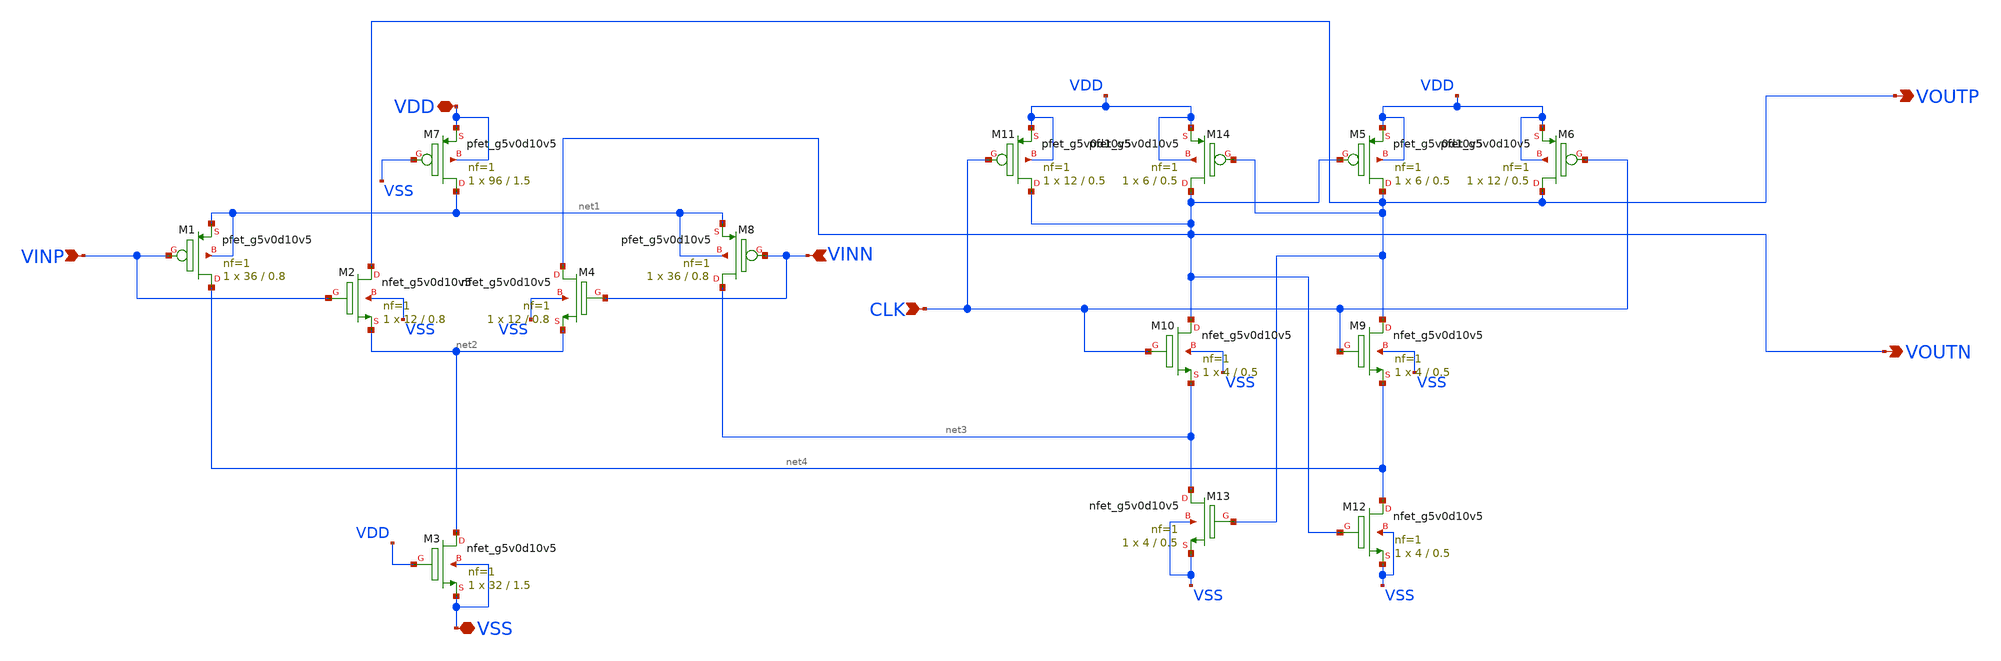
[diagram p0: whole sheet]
** sch_path: SKY130/SAR-ADC/SAR-ADC_5.0V/comp.sch
**.subckt comp VOUTP VOUTN VINP VINN CLK VDD VSS
*.opin VOUTP
*.opin VOUTN
*.ipin VINP
*.ipin VINN
*.ipin CLK
*.iopin VDD
*.iopin VSS
XM8 net3 VINN net1 net1 sky130_fd_pr__pfet_g5v0d10v5 L=0.8 W=36 nf=1 ad='int((1 + 1)/2) * 36 / 1 * 0.29'
+ as='int((1 + 2)/2) * 36 / 1 * 0.29' pd='2*int((1 + 1)/2) * (36 / 1 + 0.29)' ps='2*int((1 + 2)/2) * (36 / 1 + 0.29)'
+ nrd='0.29 / 36 ' nrs='0.29 / 36 ' sa=0 sb=0 sd=0 mult=1 m=1
XM7 net1 VSS VDD VDD sky130_fd_pr__pfet_g5v0d10v5 L=1.5 W=96 nf=1 ad='int((1 + 1)/2) * 96 / 1 * 0.29'
+ as='int((1 + 2)/2) * 96 / 1 * 0.29' pd='2*int((1 + 1)/2) * (96 / 1 + 0.29)' ps='2*int((1 + 2)/2) * (96 / 1 + 0.29)'
+ nrd='0.29 / 96 ' nrs='0.29 / 96 ' sa=0 sb=0 sd=0 mult=1 m=1
XM1 net4 VINP net1 net1 sky130_fd_pr__pfet_g5v0d10v5 L=0.8 W=36 nf=1 ad='int((1 + 1)/2) * 36 / 1 * 0.29'
+ as='int((1 + 2)/2) * 36 / 1 * 0.29' pd='2*int((1 + 1)/2) * (36 / 1 + 0.29)' ps='2*int((1 + 2)/2) * (36 / 1 + 0.29)'
+ nrd='0.29 / 36 ' nrs='0.29 / 36 ' sa=0 sb=0 sd=0 mult=1 m=1
XM2 VOUTP VINP net2 VSS sky130_fd_pr__nfet_g5v0d10v5 L=0.8 W=12 nf=1 ad='int((1 + 1)/2) * 12 / 1 * 0.29'
+ as='int((1 + 2)/2) * 12 / 1 * 0.29' pd='2*int((1 + 1)/2) * (12 / 1 + 0.29)' ps='2*int((1 + 2)/2) * (12 / 1 + 0.29)'
+ nrd='0.29 / 12 ' nrs='0.29 / 12 ' sa=0 sb=0 sd=0 mult=1 m=1
XM3 net2 VDD VSS VSS sky130_fd_pr__nfet_g5v0d10v5 L=1.5 W=32 nf=1 ad='int((1 + 1)/2) * 32 / 1 * 0.29'
+ as='int((1 + 2)/2) * 32 / 1 * 0.29' pd='2*int((1 + 1)/2) * (32 / 1 + 0.29)' ps='2*int((1 + 2)/2) * (32 / 1 + 0.29)'
+ nrd='0.29 / 32 ' nrs='0.29 / 32 ' sa=0 sb=0 sd=0 mult=1 m=1
XM4 VOUTN VINN net2 VSS sky130_fd_pr__nfet_g5v0d10v5 L=0.8 W=12 nf=1 ad='int((1 + 1)/2) * 12 / 1 * 0.29'
+ as='int((1 + 2)/2) * 12 / 1 * 0.29' pd='2*int((1 + 1)/2) * (12 / 1 + 0.29)' ps='2*int((1 + 2)/2) * (12 / 1 + 0.29)'
+ nrd='0.29 / 12 ' nrs='0.29 / 12 ' sa=0 sb=0 sd=0 mult=1 m=1
XM9 VOUTP CLK net4 VSS sky130_fd_pr__nfet_g5v0d10v5 L=0.5 W=4 nf=1 ad='int((1 + 1)/2) * 4 / 1 * 0.29'
+ as='int((1 + 2)/2) * 4 / 1 * 0.29' pd='2*int((1 + 1)/2) * (4 / 1 + 0.29)' ps='2*int((1 + 2)/2) * (4 / 1 + 0.29)'
+ nrd='0.29 / 4 ' nrs='0.29 / 4 ' sa=0 sb=0 sd=0 mult=1 m=1
XM10 VOUTN CLK net3 VSS sky130_fd_pr__nfet_g5v0d10v5 L=0.5 W=4 nf=1 ad='int((1 + 1)/2) * 4 / 1 * 0.29'
+ as='int((1 + 2)/2) * 4 / 1 * 0.29' pd='2*int((1 + 1)/2) * (4 / 1 + 0.29)' ps='2*int((1 + 2)/2) * (4 / 1 + 0.29)'
+ nrd='0.29 / 4 ' nrs='0.29 / 4 ' sa=0 sb=0 sd=0 mult=1 m=1
XM12 net4 VOUTN VSS VSS sky130_fd_pr__nfet_g5v0d10v5 L=0.5 W=4 nf=1 ad='int((1 + 1)/2) * 4 / 1 * 0.29'
+ as='int((1 + 2)/2) * 4 / 1 * 0.29' pd='2*int((1 + 1)/2) * (4 / 1 + 0.29)' ps='2*int((1 + 2)/2) * (4 / 1 + 0.29)'
+ nrd='0.29 / 4 ' nrs='0.29 / 4 ' sa=0 sb=0 sd=0 mult=1 m=1
XM13 net3 VOUTP VSS VSS sky130_fd_pr__nfet_g5v0d10v5 L=0.5 W=4 nf=1 ad='int((1 + 1)/2) * 4 / 1 * 0.29'
+ as='int((1 + 2)/2) * 4 / 1 * 0.29' pd='2*int((1 + 1)/2) * (4 / 1 + 0.29)' ps='2*int((1 + 2)/2) * (4 / 1 + 0.29)'
+ nrd='0.29 / 4 ' nrs='0.29 / 4 ' sa=0 sb=0 sd=0 mult=1 m=1
XM14 VOUTN VOUTP VDD VDD sky130_fd_pr__pfet_g5v0d10v5 L=0.5 W=6 nf=1 ad='int((1 + 1)/2) * 6 / 1 * 0.29'
+ as='int((1 + 2)/2) * 6 / 1 * 0.29' pd='2*int((1 + 1)/2) * (6 / 1 + 0.29)' ps='2*int((1 + 2)/2) * (6 / 1 + 0.29)'
+ nrd='0.29 / 6 ' nrs='0.29 / 6 ' sa=0 sb=0 sd=0 mult=1 m=1
XM11 VOUTN CLK VDD VDD sky130_fd_pr__pfet_g5v0d10v5 L=0.5 W=12 nf=1 ad='int((1 + 1)/2) * 12 / 1 * 0.29'
+ as='int((1 + 2)/2) * 12 / 1 * 0.29' pd='2*int((1 + 1)/2) * (12 / 1 + 0.29)' ps='2*int((1 + 2)/2) * (12 / 1 + 0.29)'
+ nrd='0.29 / 12 ' nrs='0.29 / 12 ' sa=0 sb=0 sd=0 mult=1 m=1
XM5 VOUTP VOUTN VDD VDD sky130_fd_pr__pfet_g5v0d10v5 L=0.5 W=6 nf=1 ad='int((1 + 1)/2) * 6 / 1 * 0.29'
+ as='int((1 + 2)/2) * 6 / 1 * 0.29' pd='2*int((1 + 1)/2) * (6 / 1 + 0.29)' ps='2*int((1 + 2)/2) * (6 / 1 + 0.29)'
+ nrd='0.29 / 6 ' nrs='0.29 / 6 ' sa=0 sb=0 sd=0 mult=1 m=1
XM6 VOUTP CLK VDD VDD sky130_fd_pr__pfet_g5v0d10v5 L=0.5 W=12 nf=1 ad='int((1 + 1)/2) * 12 / 1 * 0.29'
+ as='int((1 + 2)/2) * 12 / 1 * 0.29' pd='2*int((1 + 1)/2) * (12 / 1 + 0.29)' ps='2*int((1 + 2)/2) * (12 / 1 + 0.29)'
+ nrd='0.29 / 12 ' nrs='0.29 / 12 ' sa=0 sb=0 sd=0 mult=1 m=1
**.ends
.end
